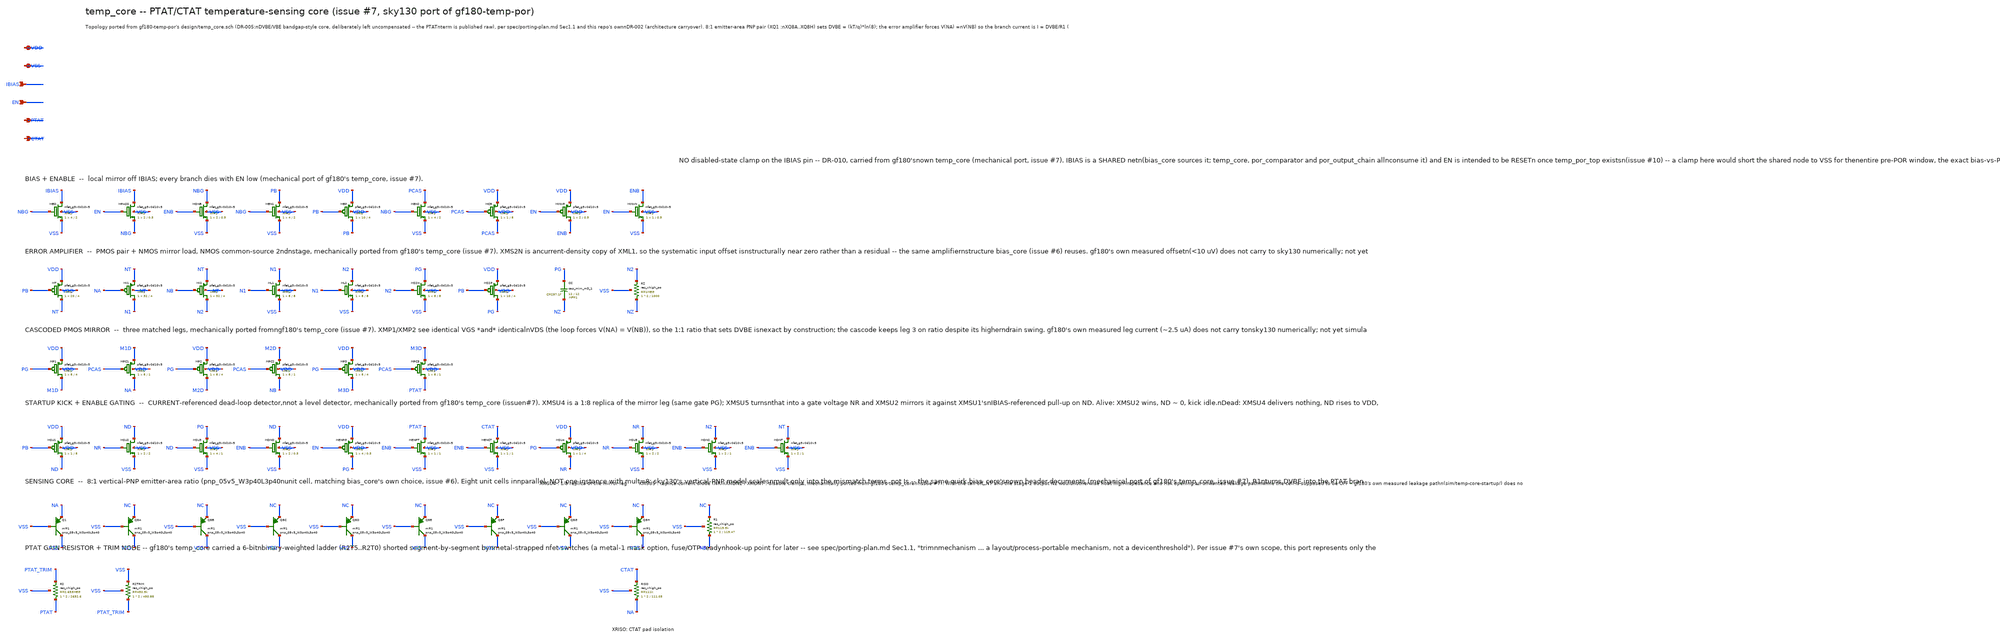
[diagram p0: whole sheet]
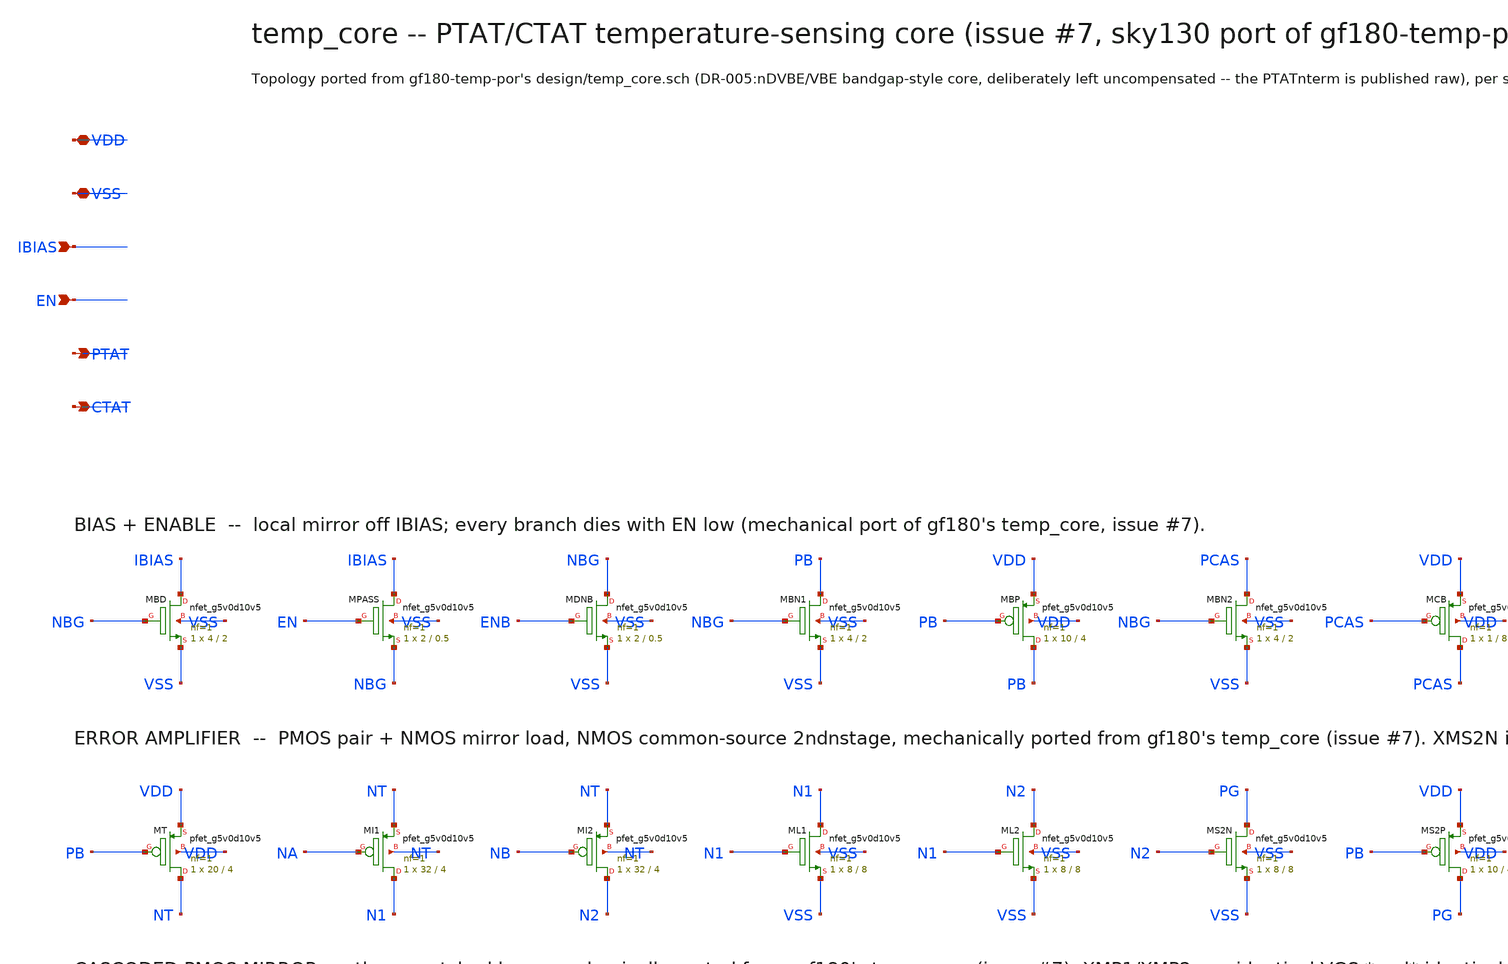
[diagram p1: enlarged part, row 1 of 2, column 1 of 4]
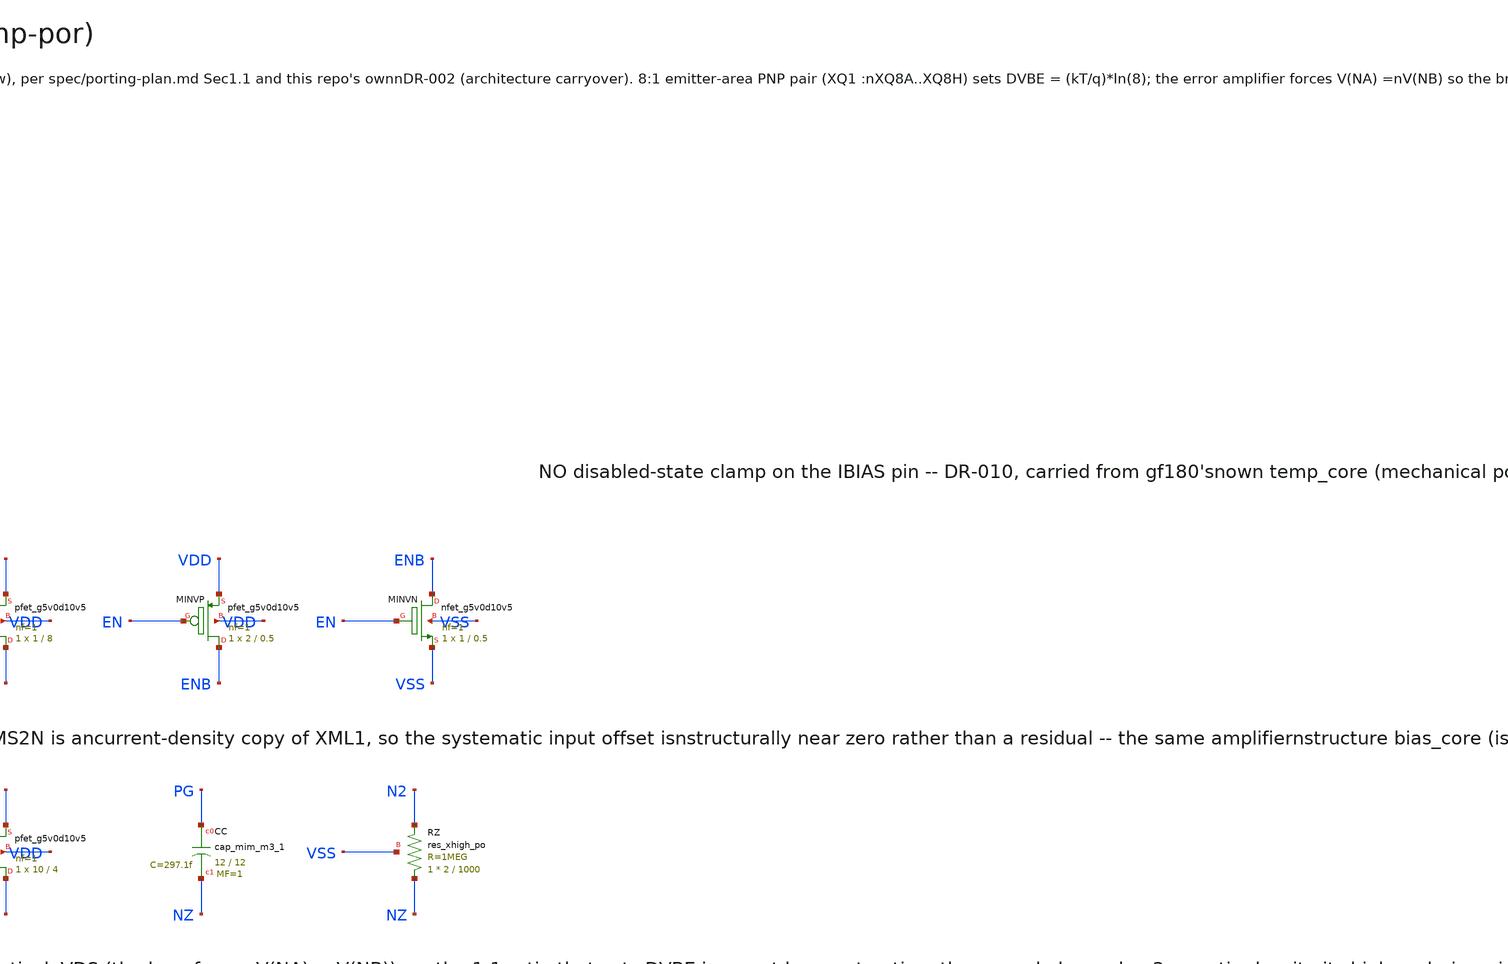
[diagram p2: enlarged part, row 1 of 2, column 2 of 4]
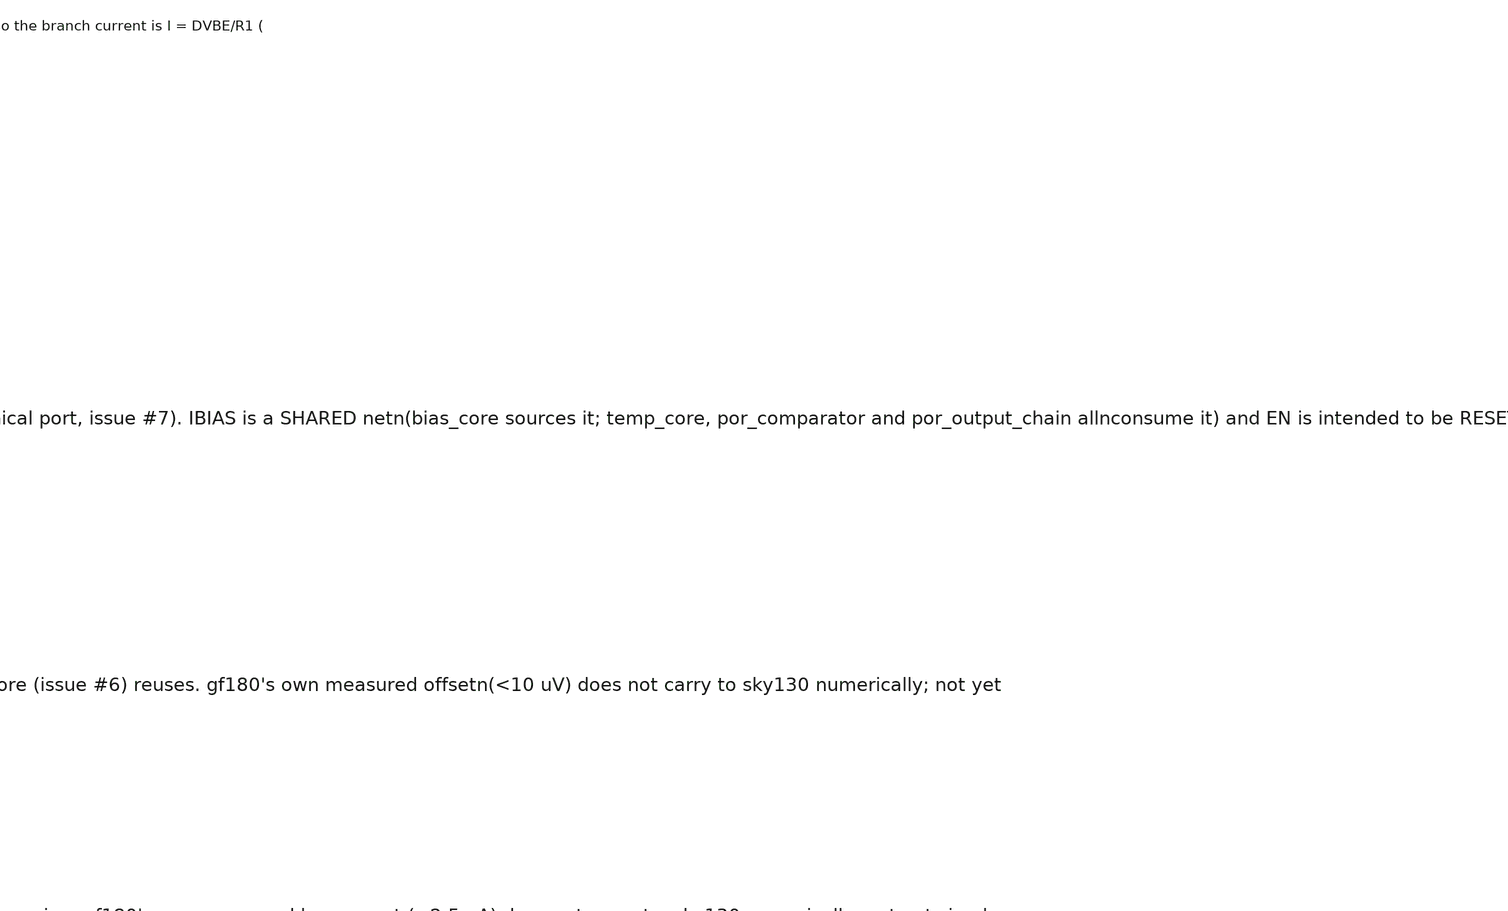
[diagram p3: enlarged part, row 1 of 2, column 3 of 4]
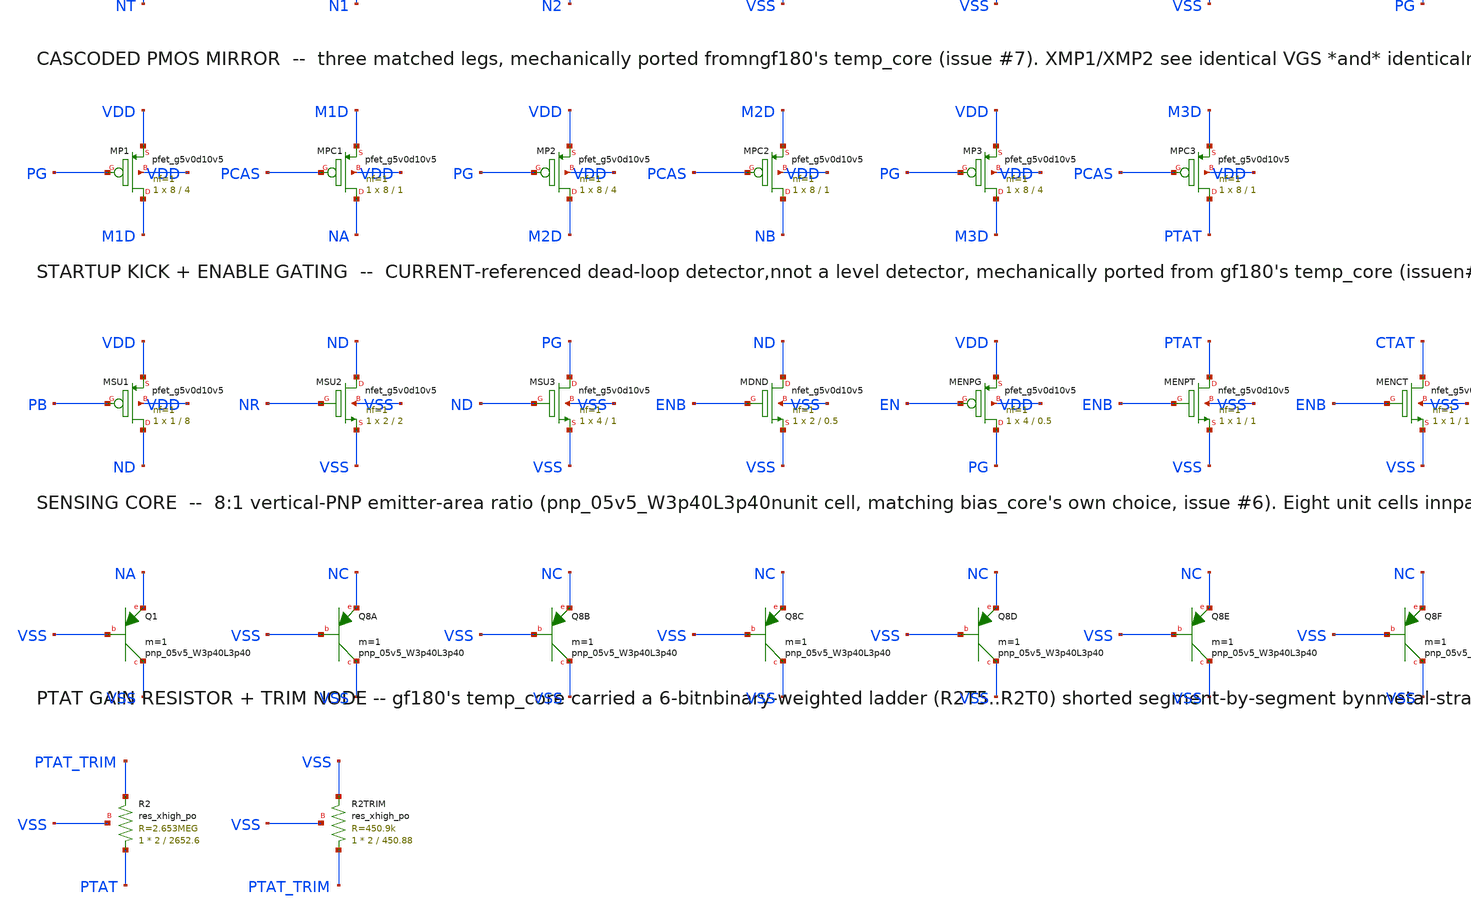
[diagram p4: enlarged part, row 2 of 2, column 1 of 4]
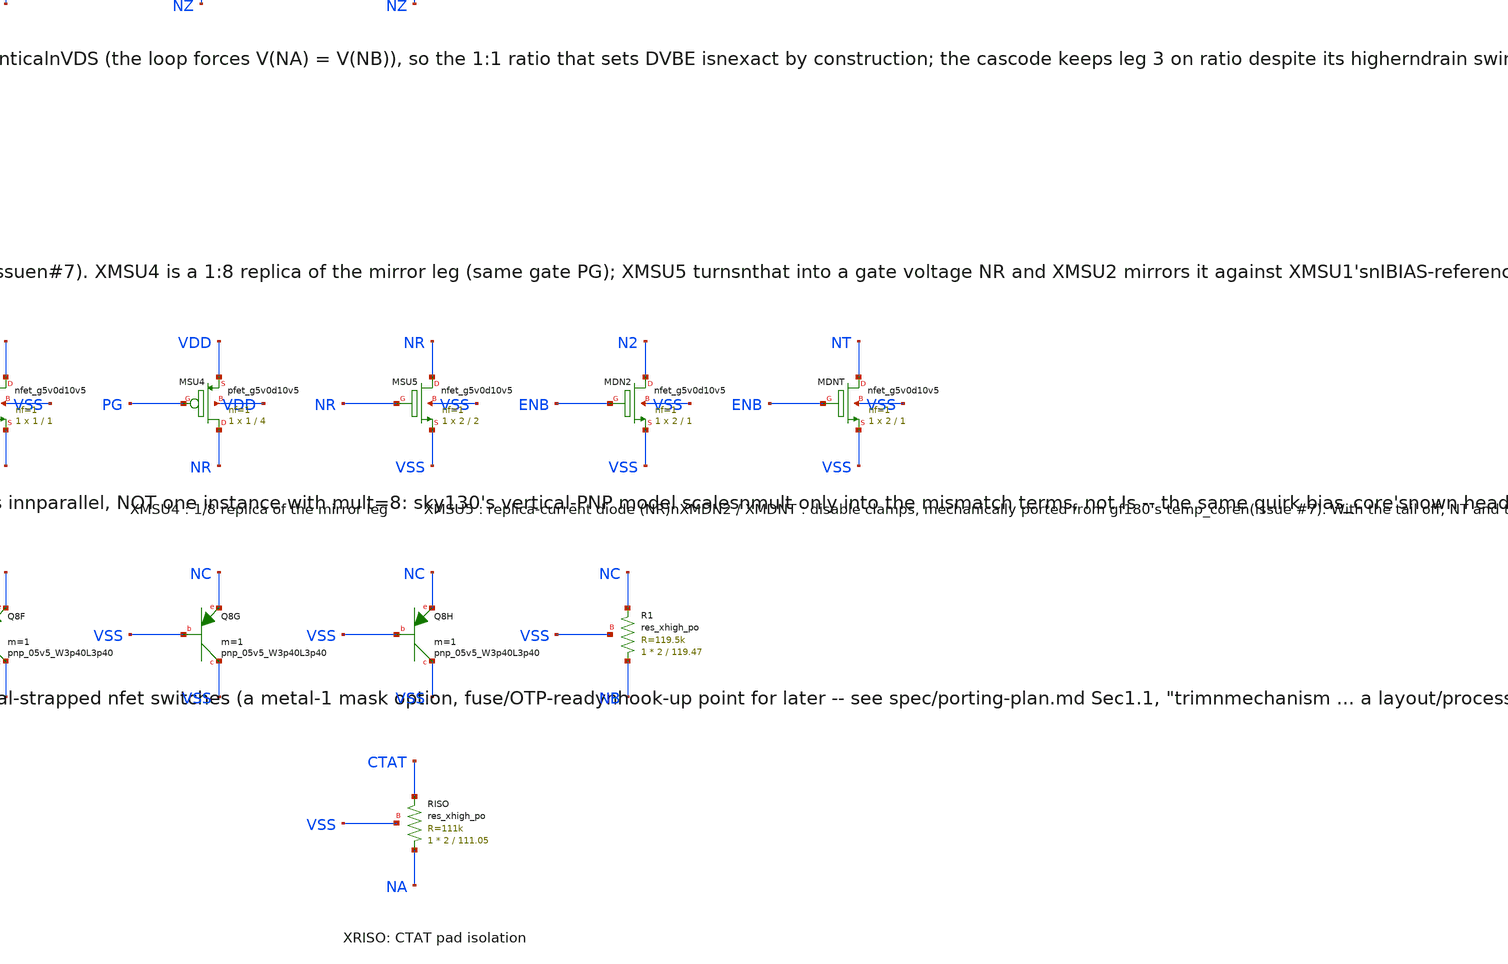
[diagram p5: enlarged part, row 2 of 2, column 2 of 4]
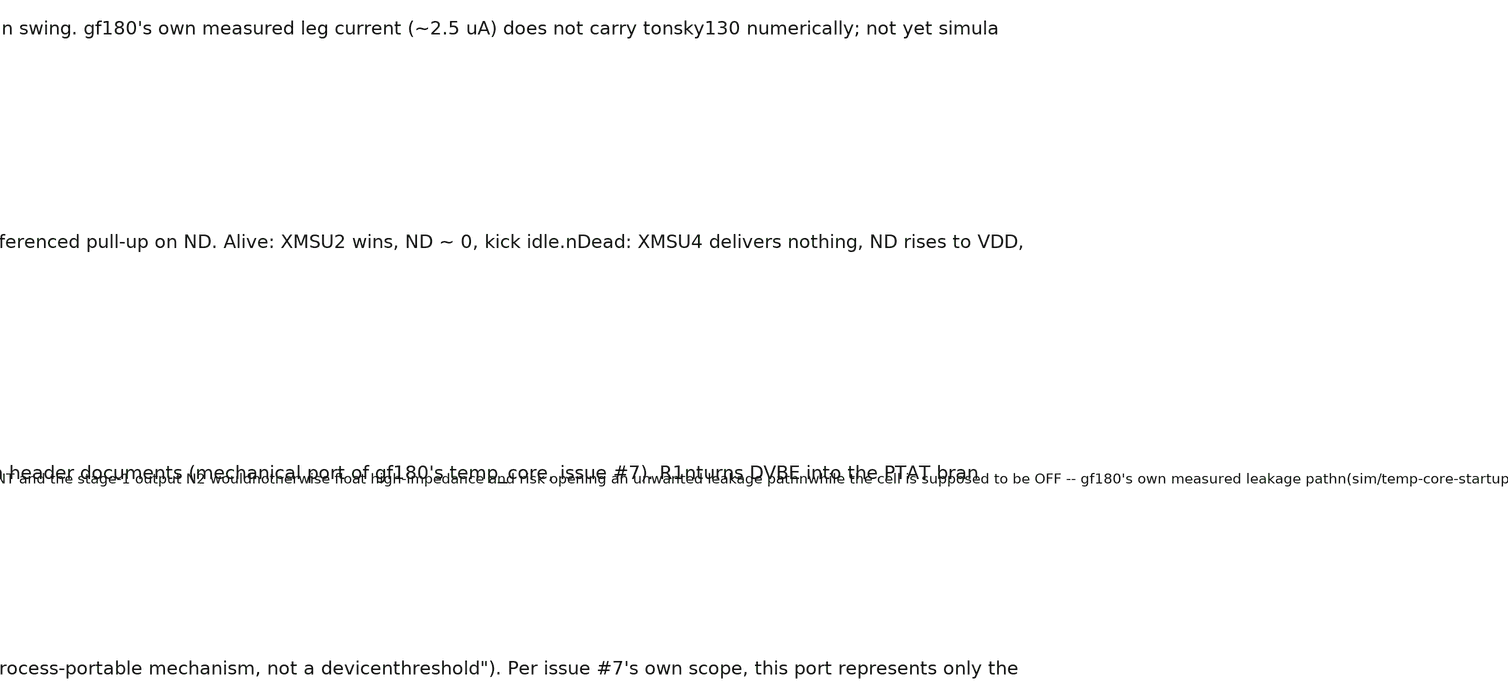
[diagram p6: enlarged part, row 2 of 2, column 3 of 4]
** sch_path: design/temp_core.sch
**.subckt temp_core VDD VSS IBIAS EN PTAT CTAT
*.iopin VDD
*.iopin VSS
*.ipin IBIAS
*.ipin EN
*.opin PTAT
*.opin CTAT
XMBD IBIAS NBG VSS VSS sky130_fd_pr__nfet_g5v0d10v5 L=2 W=4 nf=1 ad='int((1 + 1)/2) * 4 / 1 * 0.29' as='int((1 + 2)/2) * 4 / 1 * 0.29'
+ pd='2*int((1 + 1)/2) * (4 / 1 + 0.29)' ps='2*int((1 + 2)/2) * (4 / 1 + 0.29)' nrd='0.29 / 4 ' nrs='0.29 / 4 '
+ sa=0 sb=0 sd=0 mult=1 m=1
XMPASS IBIAS EN NBG VSS sky130_fd_pr__nfet_g5v0d10v5 L=0.5 W=2 nf=1 ad='int((1 + 1)/2) * 2 / 1 * 0.29'
+ as='int((1 + 2)/2) * 2 / 1 * 0.29' pd='2*int((1 + 1)/2) * (2 / 1 + 0.29)' ps='2*int((1 + 2)/2) * (2 / 1 + 0.29)'
+ nrd='0.29 / 2 ' nrs='0.29 / 2 ' sa=0 sb=0 sd=0 mult=1 m=1
XMDNB NBG ENB VSS VSS sky130_fd_pr__nfet_g5v0d10v5 L=0.5 W=2 nf=1 ad='int((1 + 1)/2) * 2 / 1 * 0.29'
+ as='int((1 + 2)/2) * 2 / 1 * 0.29' pd='2*int((1 + 1)/2) * (2 / 1 + 0.29)' ps='2*int((1 + 2)/2) * (2 / 1 + 0.29)'
+ nrd='0.29 / 2 ' nrs='0.29 / 2 ' sa=0 sb=0 sd=0 mult=1 m=1
XMBN1 PB NBG VSS VSS sky130_fd_pr__nfet_g5v0d10v5 L=2 W=4 nf=1 ad='int((1 + 1)/2) * 4 / 1 * 0.29' as='int((1 + 2)/2) * 4 / 1 * 0.29'
+ pd='2*int((1 + 1)/2) * (4 / 1 + 0.29)' ps='2*int((1 + 2)/2) * (4 / 1 + 0.29)' nrd='0.29 / 4 ' nrs='0.29 / 4 '
+ sa=0 sb=0 sd=0 mult=1 m=1
XMBP PB PB VDD VDD sky130_fd_pr__pfet_g5v0d10v5 L=4 W=10 nf=1 ad='int((1 + 1)/2) * 10 / 1 * 0.29' as='int((1 + 2)/2) * 10 / 1 * 0.29'
+ pd='2*int((1 + 1)/2) * (10 / 1 + 0.29)' ps='2*int((1 + 2)/2) * (10 / 1 + 0.29)' nrd='0.29 / 10 ' nrs='0.29 / 10 '
+ sa=0 sb=0 sd=0 mult=1 m=1
XMBN2 PCAS NBG VSS VSS sky130_fd_pr__nfet_g5v0d10v5 L=2 W=4 nf=1 ad='int((1 + 1)/2) * 4 / 1 * 0.29' as='int((1 + 2)/2) * 4 / 1 * 0.29'
+ pd='2*int((1 + 1)/2) * (4 / 1 + 0.29)' ps='2*int((1 + 2)/2) * (4 / 1 + 0.29)' nrd='0.29 / 4 ' nrs='0.29 / 4 '
+ sa=0 sb=0 sd=0 mult=1 m=1
XMCB PCAS PCAS VDD VDD sky130_fd_pr__pfet_g5v0d10v5 L=8 W=1 nf=1 ad='int((1 + 1)/2) * 1 / 1 * 0.29' as='int((1 + 2)/2) * 1 / 1 * 0.29'
+ pd='2*int((1 + 1)/2) * (1 / 1 + 0.29)' ps='2*int((1 + 2)/2) * (1 / 1 + 0.29)' nrd='0.29 / 1 ' nrs='0.29 / 1 '
+ sa=0 sb=0 sd=0 mult=1 m=1
XMINVP ENB EN VDD VDD sky130_fd_pr__pfet_g5v0d10v5 L=0.5 W=2 nf=1 ad='int((1 + 1)/2) * 2 / 1 * 0.29'
+ as='int((1 + 2)/2) * 2 / 1 * 0.29' pd='2*int((1 + 1)/2) * (2 / 1 + 0.29)' ps='2*int((1 + 2)/2) * (2 / 1 + 0.29)'
+ nrd='0.29 / 2 ' nrs='0.29 / 2 ' sa=0 sb=0 sd=0 mult=1 m=1
XMINVN ENB EN VSS VSS sky130_fd_pr__nfet_g5v0d10v5 L=0.5 W=1 nf=1 ad='int((1 + 1)/2) * 1 / 1 * 0.29'
+ as='int((1 + 2)/2) * 1 / 1 * 0.29' pd='2*int((1 + 1)/2) * (1 / 1 + 0.29)' ps='2*int((1 + 2)/2) * (1 / 1 + 0.29)'
+ nrd='0.29 / 1 ' nrs='0.29 / 1 ' sa=0 sb=0 sd=0 mult=1 m=1
XMT NT PB VDD VDD sky130_fd_pr__pfet_g5v0d10v5 L=4 W=20 nf=1 ad='int((1 + 1)/2) * 20 / 1 * 0.29' as='int((1 + 2)/2) * 20 / 1 * 0.29'
+ pd='2*int((1 + 1)/2) * (20 / 1 + 0.29)' ps='2*int((1 + 2)/2) * (20 / 1 + 0.29)' nrd='0.29 / 20 ' nrs='0.29 / 20 '
+ sa=0 sb=0 sd=0 mult=1 m=1
XMI1 N1 NA NT NT sky130_fd_pr__pfet_g5v0d10v5 L=4 W=32 nf=1 ad='int((1 + 1)/2) * 32 / 1 * 0.29' as='int((1 + 2)/2) * 32 / 1 * 0.29'
+ pd='2*int((1 + 1)/2) * (32 / 1 + 0.29)' ps='2*int((1 + 2)/2) * (32 / 1 + 0.29)' nrd='0.29 / 32 ' nrs='0.29 / 32 '
+ sa=0 sb=0 sd=0 mult=1 m=1
XMI2 N2 NB NT NT sky130_fd_pr__pfet_g5v0d10v5 L=4 W=32 nf=1 ad='int((1 + 1)/2) * 32 / 1 * 0.29' as='int((1 + 2)/2) * 32 / 1 * 0.29'
+ pd='2*int((1 + 1)/2) * (32 / 1 + 0.29)' ps='2*int((1 + 2)/2) * (32 / 1 + 0.29)' nrd='0.29 / 32 ' nrs='0.29 / 32 '
+ sa=0 sb=0 sd=0 mult=1 m=1
XML1 N1 N1 VSS VSS sky130_fd_pr__nfet_g5v0d10v5 L=8 W=8 nf=1 ad='int((1 + 1)/2) * 8 / 1 * 0.29' as='int((1 + 2)/2) * 8 / 1 * 0.29'
+ pd='2*int((1 + 1)/2) * (8 / 1 + 0.29)' ps='2*int((1 + 2)/2) * (8 / 1 + 0.29)' nrd='0.29 / 8 ' nrs='0.29 / 8 '
+ sa=0 sb=0 sd=0 mult=1 m=1
XML2 N2 N1 VSS VSS sky130_fd_pr__nfet_g5v0d10v5 L=8 W=8 nf=1 ad='int((1 + 1)/2) * 8 / 1 * 0.29' as='int((1 + 2)/2) * 8 / 1 * 0.29'
+ pd='2*int((1 + 1)/2) * (8 / 1 + 0.29)' ps='2*int((1 + 2)/2) * (8 / 1 + 0.29)' nrd='0.29 / 8 ' nrs='0.29 / 8 '
+ sa=0 sb=0 sd=0 mult=1 m=1
XMS2N PG N2 VSS VSS sky130_fd_pr__nfet_g5v0d10v5 L=8 W=8 nf=1 ad='int((1 + 1)/2) * 8 / 1 * 0.29' as='int((1 + 2)/2) * 8 / 1 * 0.29'
+ pd='2*int((1 + 1)/2) * (8 / 1 + 0.29)' ps='2*int((1 + 2)/2) * (8 / 1 + 0.29)' nrd='0.29 / 8 ' nrs='0.29 / 8 '
+ sa=0 sb=0 sd=0 mult=1 m=1
XMS2P PG PB VDD VDD sky130_fd_pr__pfet_g5v0d10v5 L=4 W=10 nf=1 ad='int((1 + 1)/2) * 10 / 1 * 0.29' as='int((1 + 2)/2) * 10 / 1 * 0.29'
+ pd='2*int((1 + 1)/2) * (10 / 1 + 0.29)' ps='2*int((1 + 2)/2) * (10 / 1 + 0.29)' nrd='0.29 / 10 ' nrs='0.29 / 10 '
+ sa=0 sb=0 sd=0 mult=1 m=1
XCC PG NZ sky130_fd_pr__cap_mim_m3_1 W=12 L=12 MF=1 m=1
XRZ NZ N2 VSS sky130_fd_pr__res_xhigh_po W=2 L=1000 mult=1 m=1
XMP1 M1D PG VDD VDD sky130_fd_pr__pfet_g5v0d10v5 L=4 W=8 nf=1 ad='int((1 + 1)/2) * 8 / 1 * 0.29' as='int((1 + 2)/2) * 8 / 1 * 0.29'
+ pd='2*int((1 + 1)/2) * (8 / 1 + 0.29)' ps='2*int((1 + 2)/2) * (8 / 1 + 0.29)' nrd='0.29 / 8 ' nrs='0.29 / 8 '
+ sa=0 sb=0 sd=0 mult=1 m=1
XMPC1 NA PCAS M1D VDD sky130_fd_pr__pfet_g5v0d10v5 L=1 W=8 nf=1 ad='int((1 + 1)/2) * 8 / 1 * 0.29' as='int((1 + 2)/2) * 8 / 1 * 0.29'
+ pd='2*int((1 + 1)/2) * (8 / 1 + 0.29)' ps='2*int((1 + 2)/2) * (8 / 1 + 0.29)' nrd='0.29 / 8 ' nrs='0.29 / 8 '
+ sa=0 sb=0 sd=0 mult=1 m=1
XMP2 M2D PG VDD VDD sky130_fd_pr__pfet_g5v0d10v5 L=4 W=8 nf=1 ad='int((1 + 1)/2) * 8 / 1 * 0.29' as='int((1 + 2)/2) * 8 / 1 * 0.29'
+ pd='2*int((1 + 1)/2) * (8 / 1 + 0.29)' ps='2*int((1 + 2)/2) * (8 / 1 + 0.29)' nrd='0.29 / 8 ' nrs='0.29 / 8 '
+ sa=0 sb=0 sd=0 mult=1 m=1
XMPC2 NB PCAS M2D VDD sky130_fd_pr__pfet_g5v0d10v5 L=1 W=8 nf=1 ad='int((1 + 1)/2) * 8 / 1 * 0.29' as='int((1 + 2)/2) * 8 / 1 * 0.29'
+ pd='2*int((1 + 1)/2) * (8 / 1 + 0.29)' ps='2*int((1 + 2)/2) * (8 / 1 + 0.29)' nrd='0.29 / 8 ' nrs='0.29 / 8 '
+ sa=0 sb=0 sd=0 mult=1 m=1
XMP3 M3D PG VDD VDD sky130_fd_pr__pfet_g5v0d10v5 L=4 W=8 nf=1 ad='int((1 + 1)/2) * 8 / 1 * 0.29' as='int((1 + 2)/2) * 8 / 1 * 0.29'
+ pd='2*int((1 + 1)/2) * (8 / 1 + 0.29)' ps='2*int((1 + 2)/2) * (8 / 1 + 0.29)' nrd='0.29 / 8 ' nrs='0.29 / 8 '
+ sa=0 sb=0 sd=0 mult=1 m=1
XMPC3 PTAT PCAS M3D VDD sky130_fd_pr__pfet_g5v0d10v5 L=1 W=8 nf=1 ad='int((1 + 1)/2) * 8 / 1 * 0.29'
+ as='int((1 + 2)/2) * 8 / 1 * 0.29' pd='2*int((1 + 1)/2) * (8 / 1 + 0.29)' ps='2*int((1 + 2)/2) * (8 / 1 + 0.29)'
+ nrd='0.29 / 8 ' nrs='0.29 / 8 ' sa=0 sb=0 sd=0 mult=1 m=1
XMSU1 ND PB VDD VDD sky130_fd_pr__pfet_g5v0d10v5 L=8 W=1 nf=1 ad='int((1 + 1)/2) * 1 / 1 * 0.29' as='int((1 + 2)/2) * 1 / 1 * 0.29'
+ pd='2*int((1 + 1)/2) * (1 / 1 + 0.29)' ps='2*int((1 + 2)/2) * (1 / 1 + 0.29)' nrd='0.29 / 1 ' nrs='0.29 / 1 '
+ sa=0 sb=0 sd=0 mult=1 m=1
XMSU2 ND NR VSS VSS sky130_fd_pr__nfet_g5v0d10v5 L=2 W=2 nf=1 ad='int((1 + 1)/2) * 2 / 1 * 0.29' as='int((1 + 2)/2) * 2 / 1 * 0.29'
+ pd='2*int((1 + 1)/2) * (2 / 1 + 0.29)' ps='2*int((1 + 2)/2) * (2 / 1 + 0.29)' nrd='0.29 / 2 ' nrs='0.29 / 2 '
+ sa=0 sb=0 sd=0 mult=1 m=1
XMSU3 PG ND VSS VSS sky130_fd_pr__nfet_g5v0d10v5 L=1 W=4 nf=1 ad='int((1 + 1)/2) * 4 / 1 * 0.29' as='int((1 + 2)/2) * 4 / 1 * 0.29'
+ pd='2*int((1 + 1)/2) * (4 / 1 + 0.29)' ps='2*int((1 + 2)/2) * (4 / 1 + 0.29)' nrd='0.29 / 4 ' nrs='0.29 / 4 '
+ sa=0 sb=0 sd=0 mult=1 m=1
XMDND ND ENB VSS VSS sky130_fd_pr__nfet_g5v0d10v5 L=0.5 W=2 nf=1 ad='int((1 + 1)/2) * 2 / 1 * 0.29' as='int((1 + 2)/2) * 2 / 1 * 0.29'
+ pd='2*int((1 + 1)/2) * (2 / 1 + 0.29)' ps='2*int((1 + 2)/2) * (2 / 1 + 0.29)' nrd='0.29 / 2 ' nrs='0.29 / 2 '
+ sa=0 sb=0 sd=0 mult=1 m=1
XMENPG PG EN VDD VDD sky130_fd_pr__pfet_g5v0d10v5 L=0.5 W=4 nf=1 ad='int((1 + 1)/2) * 4 / 1 * 0.29' as='int((1 + 2)/2) * 4 / 1 * 0.29'
+ pd='2*int((1 + 1)/2) * (4 / 1 + 0.29)' ps='2*int((1 + 2)/2) * (4 / 1 + 0.29)' nrd='0.29 / 4 ' nrs='0.29 / 4 '
+ sa=0 sb=0 sd=0 mult=1 m=1
XMENPT PTAT ENB VSS VSS sky130_fd_pr__nfet_g5v0d10v5 L=1 W=1 nf=1 ad='int((1 + 1)/2) * 1 / 1 * 0.29'
+ as='int((1 + 2)/2) * 1 / 1 * 0.29' pd='2*int((1 + 1)/2) * (1 / 1 + 0.29)' ps='2*int((1 + 2)/2) * (1 / 1 + 0.29)'
+ nrd='0.29 / 1 ' nrs='0.29 / 1 ' sa=0 sb=0 sd=0 mult=1 m=1
XMENCT CTAT ENB VSS VSS sky130_fd_pr__nfet_g5v0d10v5 L=1 W=1 nf=1 ad='int((1 + 1)/2) * 1 / 1 * 0.29'
+ as='int((1 + 2)/2) * 1 / 1 * 0.29' pd='2*int((1 + 1)/2) * (1 / 1 + 0.29)' ps='2*int((1 + 2)/2) * (1 / 1 + 0.29)'
+ nrd='0.29 / 1 ' nrs='0.29 / 1 ' sa=0 sb=0 sd=0 mult=1 m=1
XMSU4 NR PG VDD VDD sky130_fd_pr__pfet_g5v0d10v5 L=4 W=1 nf=1 ad='int((1 + 1)/2) * 1 / 1 * 0.29' as='int((1 + 2)/2) * 1 / 1 * 0.29'
+ pd='2*int((1 + 1)/2) * (1 / 1 + 0.29)' ps='2*int((1 + 2)/2) * (1 / 1 + 0.29)' nrd='0.29 / 1 ' nrs='0.29 / 1 '
+ sa=0 sb=0 sd=0 mult=1 m=1
XMSU5 NR NR VSS VSS sky130_fd_pr__nfet_g5v0d10v5 L=2 W=2 nf=1 ad='int((1 + 1)/2) * 2 / 1 * 0.29' as='int((1 + 2)/2) * 2 / 1 * 0.29'
+ pd='2*int((1 + 1)/2) * (2 / 1 + 0.29)' ps='2*int((1 + 2)/2) * (2 / 1 + 0.29)' nrd='0.29 / 2 ' nrs='0.29 / 2 '
+ sa=0 sb=0 sd=0 mult=1 m=1
XMDN2 N2 ENB VSS VSS sky130_fd_pr__nfet_g5v0d10v5 L=1 W=2 nf=1 ad='int((1 + 1)/2) * 2 / 1 * 0.29' as='int((1 + 2)/2) * 2 / 1 * 0.29'
+ pd='2*int((1 + 1)/2) * (2 / 1 + 0.29)' ps='2*int((1 + 2)/2) * (2 / 1 + 0.29)' nrd='0.29 / 2 ' nrs='0.29 / 2 '
+ sa=0 sb=0 sd=0 mult=1 m=1
XMDNT NT ENB VSS VSS sky130_fd_pr__nfet_g5v0d10v5 L=1 W=2 nf=1 ad='int((1 + 1)/2) * 2 / 1 * 0.29' as='int((1 + 2)/2) * 2 / 1 * 0.29'
+ pd='2*int((1 + 1)/2) * (2 / 1 + 0.29)' ps='2*int((1 + 2)/2) * (2 / 1 + 0.29)' nrd='0.29 / 2 ' nrs='0.29 / 2 '
+ sa=0 sb=0 sd=0 mult=1 m=1
XQ1 VSS VSS NA sky130_fd_pr__pnp_05v5_W3p40L3p40 m=1
XQ8A VSS VSS NC sky130_fd_pr__pnp_05v5_W3p40L3p40 m=1
XQ8B VSS VSS NC sky130_fd_pr__pnp_05v5_W3p40L3p40 m=1
XQ8C VSS VSS NC sky130_fd_pr__pnp_05v5_W3p40L3p40 m=1
XQ8D VSS VSS NC sky130_fd_pr__pnp_05v5_W3p40L3p40 m=1
XQ8E VSS VSS NC sky130_fd_pr__pnp_05v5_W3p40L3p40 m=1
XQ8F VSS VSS NC sky130_fd_pr__pnp_05v5_W3p40L3p40 m=1
XQ8G VSS VSS NC sky130_fd_pr__pnp_05v5_W3p40L3p40 m=1
XQ8H VSS VSS NC sky130_fd_pr__pnp_05v5_W3p40L3p40 m=1
XR1 NB NC VSS sky130_fd_pr__res_xhigh_po W=2 L=119.47 mult=1 m=1
XR2 PTAT PTAT_TRIM VSS sky130_fd_pr__res_xhigh_po W=2 L=2652.6 mult=1 m=1
XR2TRIM PTAT_TRIM VSS VSS sky130_fd_pr__res_xhigh_po W=2 L=450.88 mult=1 m=1
XRISO NA CTAT VSS sky130_fd_pr__res_xhigh_po W=2 L=111.05 mult=1 m=1
**.ends
.end
